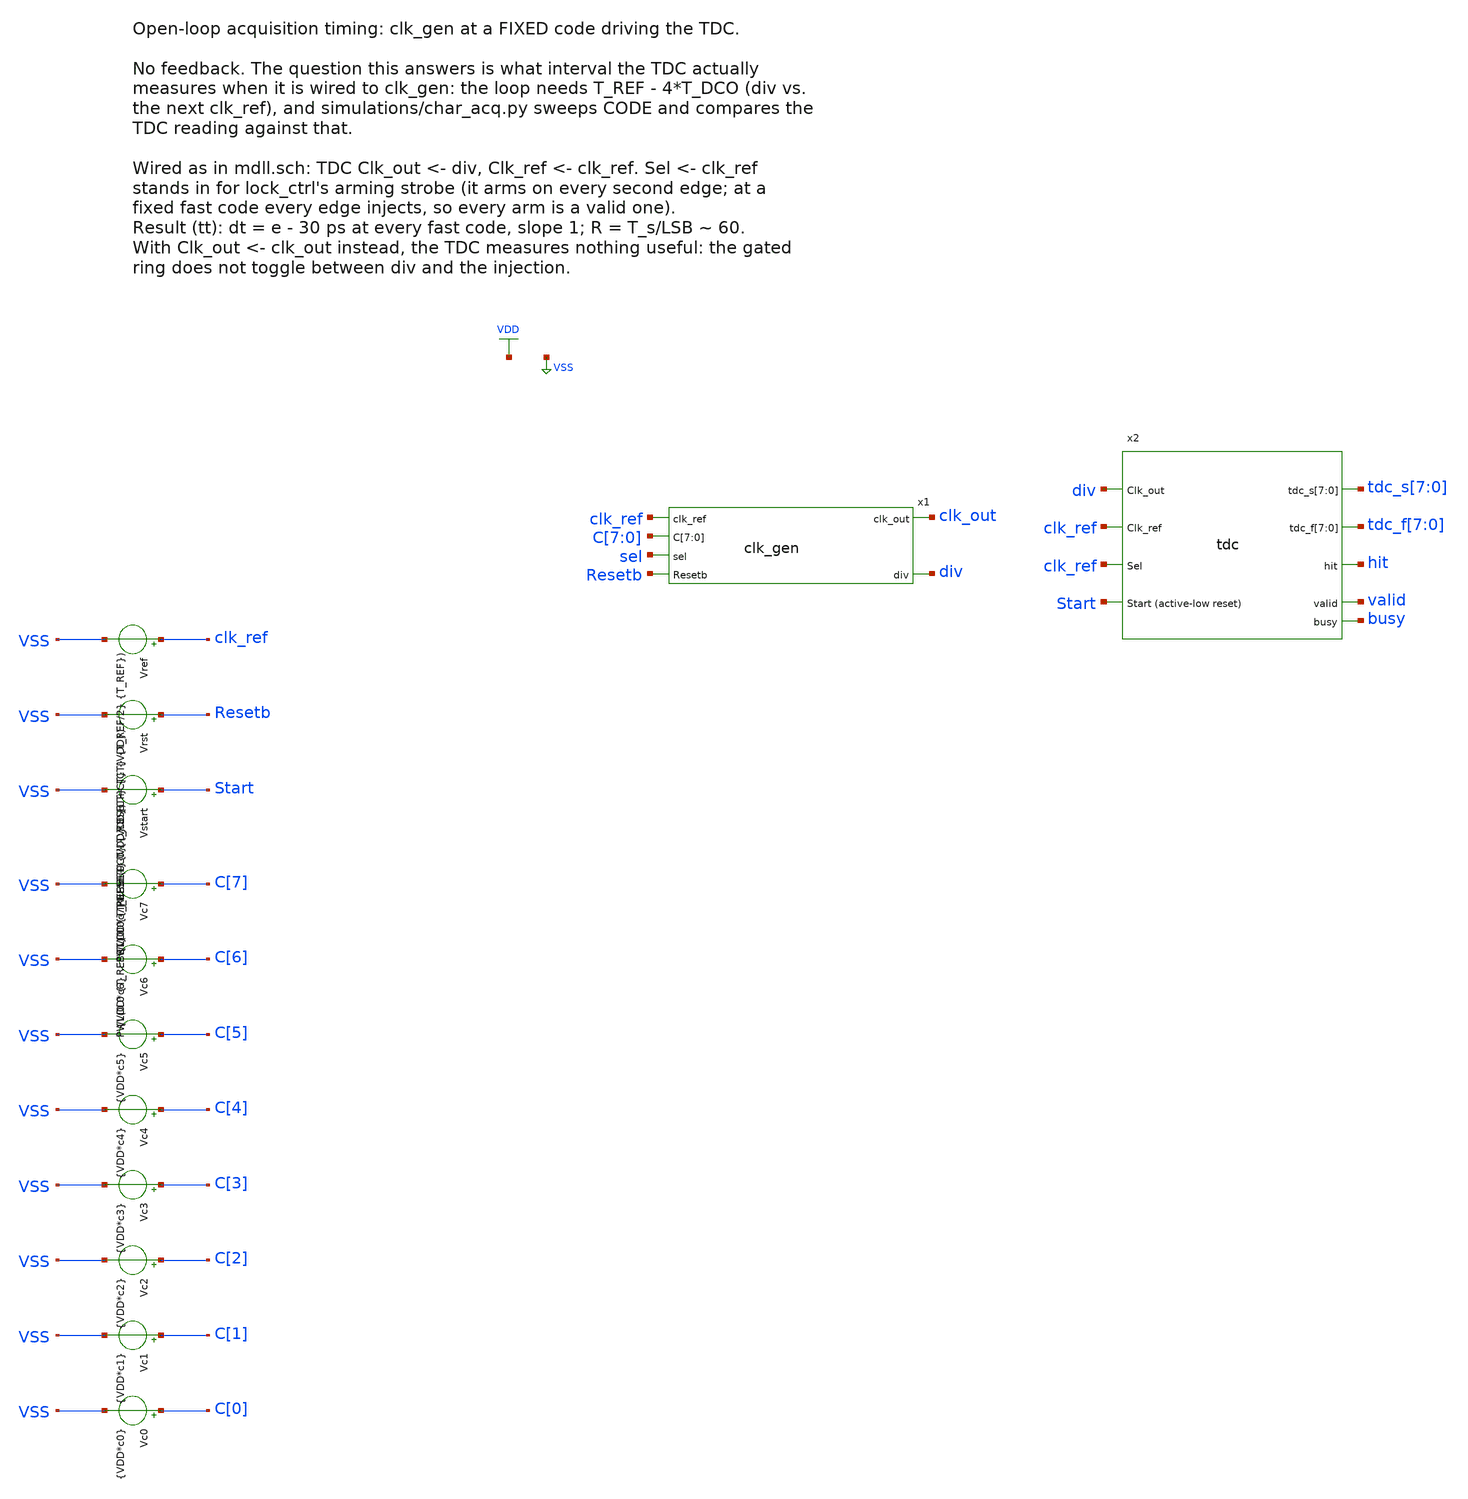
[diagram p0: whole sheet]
** sch_path: TPU5555-main/mdll/mixed_signal_design_blocks/test_acq.sch


* This block is tcleval()'d: xschem runs it through tcl subst when writing the
* netlist. A stray dollar sign or open bracket is therefore a tcl error, and a
* failed tcleval turns the WHOLE block into a single question mark, silently.
* The root Makefile greps the netlist for it. See CLAUDE.md.

* Generated models, rebuilt by the Netlist button. rc=0 is success; otherwise
* read the named log and expect a stale model below.
* mk dco_decode.spice rc=[file mkdir $env(MSDB_ROOT)/build][catch {exec make -s -C $env(MSDB_ROOT)/clk_gen
*+ simulations/dco_decode.spice >& $env(MSDB_ROOT)/build/mk_dco_decode.log}]
* mk counter.spice rc=[catch {exec make -s -C $env(MSDB_ROOT)/tdc simulations/counter.spice >& $env(MSDB_ROOT)/build/mk_counter.log}]

.LIB cornerMOSlv.lib mos_tt
.OPTIONS KLU
.INCLUDE sg13g2_stdcell.spice
.INCLUDE custom_stdcell.spice
.INCLUDE $env(MSDB_ROOT)/clk_gen/simulations/dco_decode.spice
.INCLUDE $env(MSDB_ROOT)/tdc/simulations/counter.spice

* Handed to the CODE block as an ngspice variable: that block names bus bits,
* so it cannot be tcleval'd. setcs, not set: set lower-cases its value.
.control
  setcs rawfile = $env(MSDB_ROOT)/simulations/test_acq.raw
.endc
.PARAM VDD=1.2
.PARAM T_REF=10n
.PARAM CT=50p
.PARAM T_RESET={T_REF + 0.1n}
.PARAM CODE=0
.TEMP 27

* CODE bit by bit for Vc7..Vc0 (ngspice .param has no bitwise operators).
.param c0={int(CODE/1)-2*int(CODE/2)}
.param c1={int(CODE/2)-2*int(CODE/4)}
.param c2={int(CODE/4)-2*int(CODE/8)}
.param c3={int(CODE/8)-2*int(CODE/16)}
.param c4={int(CODE/16)-2*int(CODE/32)}
.param c5={int(CODE/32)-2*int(CODE/64)}
.param c6={int(CODE/64)-2*int(CODE/128)}
.param c7={int(CODE/128)-2*int(CODE/256)}


**.subckt test_acq
x1 clk_ref C[7] C[6] C[5] C[4] C[3] C[2] C[1] C[0] clk_out sel Resetb div clk_gen
x2 div clk_ref clk_ref Start tdc_s[7] tdc_s[6] tdc_s[5] tdc_s[4] tdc_s[3] tdc_s[2] tdc_s[1] tdc_s[0]
+ tdc_f[7] tdc_f[6] tdc_f[5] tdc_f[4] tdc_f[3] tdc_f[2] tdc_f[1] tdc_f[0] hit valid busy VDD VSS tdc
Vref clk_ref VSS PULSE(0 {VDD} 0 {CT} {CT} {T_REF/2} {T_REF})
Vrst Resetb VSS PWL(0 0 {T_RESET} 0 {T_RESET+CT} {VDD})
Vstart Start VSS PWL(0 0 {T_RESET} 0 {T_RESET+CT} {VDD})
Vc7 C[7] VSS {VDD*c7}
Vc6 C[6] VSS {VDD*c6}
Vc5 C[5] VSS {VDD*c5}
Vc4 C[4] VSS {VDD*c4}
Vc3 C[3] VSS {VDD*c3}
Vc2 C[2] VSS {VDD*c2}
Vc1 C[1] VSS {VDD*c1}
Vc0 C[0] VSS {VDD*c0}
**** begin user architecture code


VVDD VDD 0 DC {VDD}
VVSS VSS 0 0
.control
  set filetype=ascii
  save clk_ref clk_out div sel Resetb Start hit valid busy
  save tdc_s[7] tdc_s[6] tdc_s[5] tdc_s[4] tdc_s[3] tdc_s[2] tdc_s[1] tdc_s[0]
  save tdc_f[7] tdc_f[6] tdc_f[5] tdc_f[4] tdc_f[3] tdc_f[2] tdc_f[1] tdc_f[0]
  save x2.OS x2.OF x2.Reset x2.Detect x2.hit_raw
  tran 5p 120n
  write $rawfile
  quit
.endc


**** end user architecture code
**.ends
.GLOBAL VDD
.GLOBAL VSS
.end
